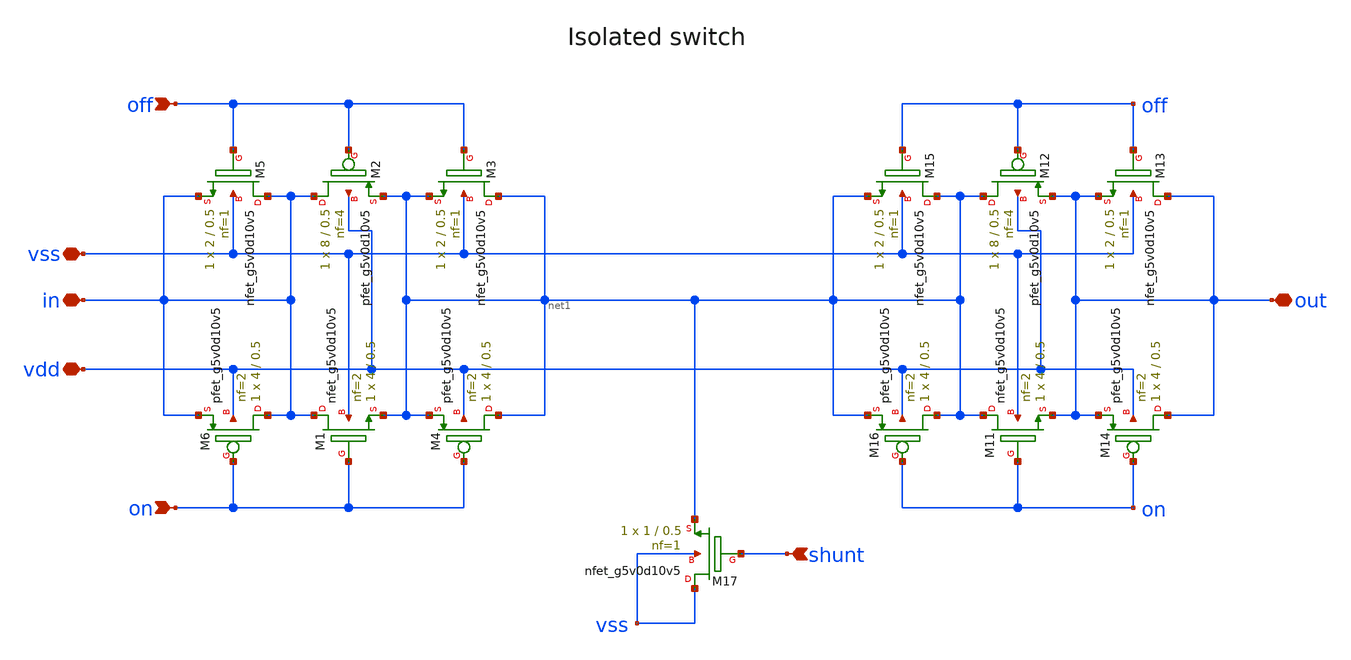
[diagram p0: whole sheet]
** sch_path: analog/repairs/cdac_tap_fix/project/dependencies/sky130_ef_ip__analog_switches/xschem/isolated_switch_2.sch
**.subckt isolated_switch_2 on out vdd vss in off shunt
*.ipin on
*.iopin out
*.iopin vdd
*.iopin vss
*.iopin in
*.ipin off
*.ipin shunt
XM1 in on net1 vss sky130_fd_pr__nfet_g5v0d10v5 L=0.5 W=4 nf=2 ad='int((nf+1)/2) * W/nf * 0.29' as='int((nf+2)/2) * W/nf * 0.29'
+ pd='2*int((nf+1)/2) * (W/nf + 0.29)' ps='2*int((nf+2)/2) * (W/nf + 0.29)' nrd='0.29 / W' nrs='0.29 / W'
+ sa=0 sb=0 sd=0 mult=1 m=1
XM2 in off net1 vdd sky130_fd_pr__pfet_g5v0d10v5 L=0.5 W=8 nf=4 ad='int((nf+1)/2) * W/nf * 0.29' as='int((nf+2)/2) * W/nf * 0.29'
+ pd='2*int((nf+1)/2) * (W/nf + 0.29)' ps='2*int((nf+2)/2) * (W/nf + 0.29)' nrd='0.29 / W' nrs='0.29 / W'
+ sa=0 sb=0 sd=0 mult=1 m=1
XM3 net1 off net1 vss sky130_fd_pr__nfet_g5v0d10v5 L=0.5 W=2 nf=1 ad='int((nf+1)/2) * W/nf * 0.29' as='int((nf+2)/2) * W/nf * 0.29'
+ pd='2*int((nf+1)/2) * (W/nf + 0.29)' ps='2*int((nf+2)/2) * (W/nf + 0.29)' nrd='0.29 / W' nrs='0.29 / W'
+ sa=0 sb=0 sd=0 mult=1 m=1
XM4 net1 on net1 vdd sky130_fd_pr__pfet_g5v0d10v5 L=0.5 W=4 nf=2 ad='int((nf+1)/2) * W/nf * 0.29' as='int((nf+2)/2) * W/nf * 0.29'
+ pd='2*int((nf+1)/2) * (W/nf + 0.29)' ps='2*int((nf+2)/2) * (W/nf + 0.29)' nrd='0.29 / W' nrs='0.29 / W'
+ sa=0 sb=0 sd=0 mult=1 m=1
XM5 in off in vss sky130_fd_pr__nfet_g5v0d10v5 L=0.5 W=2 nf=1 ad='int((nf+1)/2) * W/nf * 0.29' as='int((nf+2)/2) * W/nf * 0.29'
+ pd='2*int((nf+1)/2) * (W/nf + 0.29)' ps='2*int((nf+2)/2) * (W/nf + 0.29)' nrd='0.29 / W' nrs='0.29 / W'
+ sa=0 sb=0 sd=0 mult=1 m=1
XM6 in on in vdd sky130_fd_pr__pfet_g5v0d10v5 L=0.5 W=4 nf=2 ad='int((nf+1)/2) * W/nf * 0.29' as='int((nf+2)/2) * W/nf * 0.29'
+ pd='2*int((nf+1)/2) * (W/nf + 0.29)' ps='2*int((nf+2)/2) * (W/nf + 0.29)' nrd='0.29 / W' nrs='0.29 / W'
+ sa=0 sb=0 sd=0 mult=1 m=1
XM11 net1 on out vss sky130_fd_pr__nfet_g5v0d10v5 L=0.5 W=4 nf=2 ad='int((nf+1)/2) * W/nf * 0.29' as='int((nf+2)/2) * W/nf * 0.29'
+ pd='2*int((nf+1)/2) * (W/nf + 0.29)' ps='2*int((nf+2)/2) * (W/nf + 0.29)' nrd='0.29 / W' nrs='0.29 / W'
+ sa=0 sb=0 sd=0 mult=1 m=1
XM12 net1 off out vdd sky130_fd_pr__pfet_g5v0d10v5 L=0.5 W=8 nf=4 ad='int((nf+1)/2) * W/nf * 0.29' as='int((nf+2)/2) * W/nf * 0.29'
+ pd='2*int((nf+1)/2) * (W/nf + 0.29)' ps='2*int((nf+2)/2) * (W/nf + 0.29)' nrd='0.29 / W' nrs='0.29 / W'
+ sa=0 sb=0 sd=0 mult=1 m=1
XM13 out off out vss sky130_fd_pr__nfet_g5v0d10v5 L=0.5 W=2 nf=1 ad='int((nf+1)/2) * W/nf * 0.29' as='int((nf+2)/2) * W/nf * 0.29'
+ pd='2*int((nf+1)/2) * (W/nf + 0.29)' ps='2*int((nf+2)/2) * (W/nf + 0.29)' nrd='0.29 / W' nrs='0.29 / W'
+ sa=0 sb=0 sd=0 mult=1 m=1
XM14 out on out vdd sky130_fd_pr__pfet_g5v0d10v5 L=0.5 W=4 nf=2 ad='int((nf+1)/2) * W/nf * 0.29' as='int((nf+2)/2) * W/nf * 0.29'
+ pd='2*int((nf+1)/2) * (W/nf + 0.29)' ps='2*int((nf+2)/2) * (W/nf + 0.29)' nrd='0.29 / W' nrs='0.29 / W'
+ sa=0 sb=0 sd=0 mult=1 m=1
XM15 net1 off net1 vss sky130_fd_pr__nfet_g5v0d10v5 L=0.5 W=2 nf=1 ad='int((nf+1)/2) * W/nf * 0.29' as='int((nf+2)/2) * W/nf * 0.29'
+ pd='2*int((nf+1)/2) * (W/nf + 0.29)' ps='2*int((nf+2)/2) * (W/nf + 0.29)' nrd='0.29 / W' nrs='0.29 / W'
+ sa=0 sb=0 sd=0 mult=1 m=1
XM16 net1 on net1 vdd sky130_fd_pr__pfet_g5v0d10v5 L=0.5 W=4 nf=2 ad='int((nf+1)/2) * W/nf * 0.29' as='int((nf+2)/2) * W/nf * 0.29'
+ pd='2*int((nf+1)/2) * (W/nf + 0.29)' ps='2*int((nf+2)/2) * (W/nf + 0.29)' nrd='0.29 / W' nrs='0.29 / W'
+ sa=0 sb=0 sd=0 mult=1 m=1
XM17 vss shunt net1 vss sky130_fd_pr__nfet_g5v0d10v5 L=0.5 W=1 nf=1 ad='int((nf+1)/2) * W/nf * 0.29'
+ as='int((nf+2)/2) * W/nf * 0.29' pd='2*int((nf+1)/2) * (W/nf + 0.29)' ps='2*int((nf+2)/2) * (W/nf + 0.29)'
+ nrd='0.29 / W' nrs='0.29 / W' sa=0 sb=0 sd=0 mult=1 m=1
**.ends
.end
